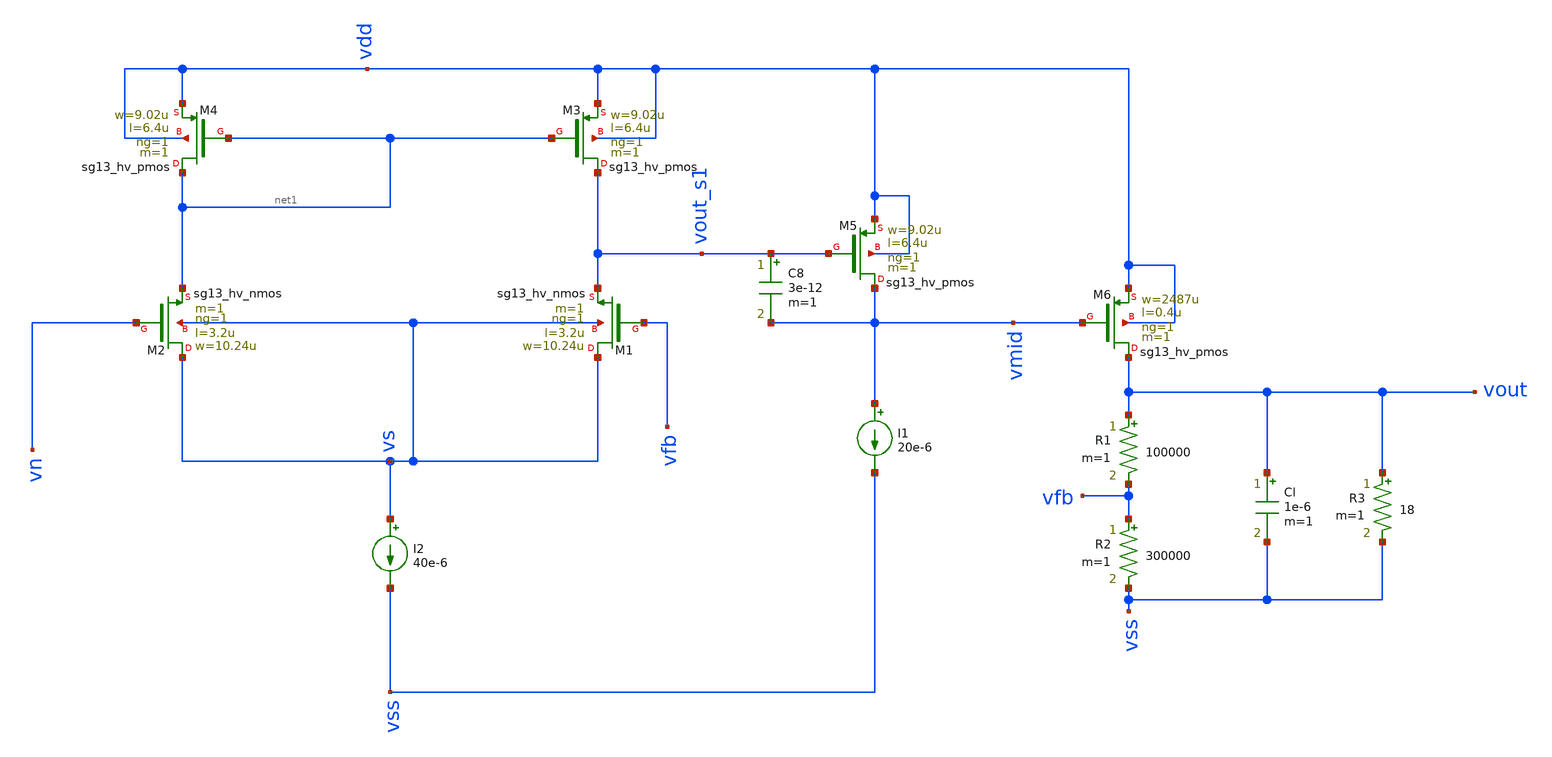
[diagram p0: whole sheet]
** sch_path: test/sstadex/xschem/ldo_sim_ihp.sch
**.subckt ldo_sim_ihp
I2 vs vss 40e-6
I1 vmid vss 20e-6
C8 vout_s1 vmid 3e-12 m=1
R1 vout vfb 100000 m=1
R2 vfb vss 300000 m=1
Cl vout vss 1e-6 m=1
R3 vout vss 18 m=1
XM1 vs vfb vout_s1 vs sg13_hv_nmos w=10.24u l=3.2u ng=1 m=1 mm_ok=1
XM2 vs vn net1 vs sg13_hv_nmos w=10.24u l=3.2u ng=1 m=1 mm_ok=1
XM3 vout_s1 net1 vdd vdd sg13_hv_pmos w=9.02u l=6.4u ng=1 m=1 mm_ok=1
XM4 net1 net1 vdd vdd sg13_hv_pmos w=9.02u l=6.4u ng=1 m=1 mm_ok=1
XM5 vmid vout_s1 vdd vdd sg13_hv_pmos w=9.02u l=6.4u ng=1 m=1 mm_ok=1
XM6 vout vmid vdd vdd sg13_hv_pmos w=2487u l=0.4u ng=1 m=1 mm_ok=1
**** begin user architecture code



.lib /opt/pdks/ihp-sg13g2/libs.tech/ngspice/models/cornerMOShv.lib mos_tt

Vref vn 0 1.35
Vdd vdd 0 3.3 ac 1
Vss vss 0 0

.control
ac dec 10 1 100G
plot vdb(vout)
plot phase(vout)
op
print vout vmid vout_s1 vs
.endc



**** end user architecture code
**.ends
.end
